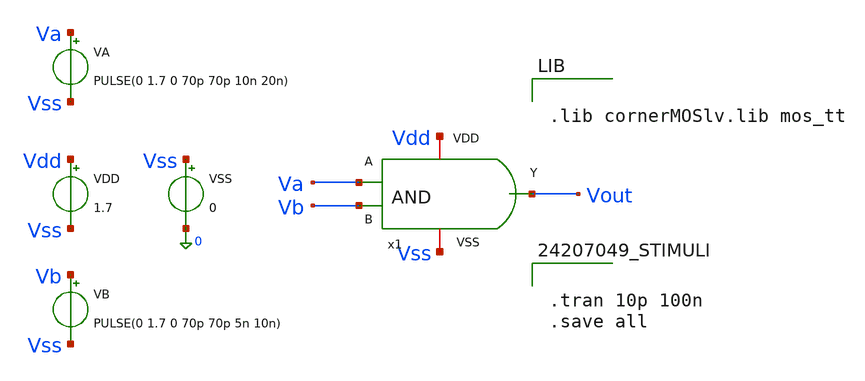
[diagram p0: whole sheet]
** sch_path: logic_gate/AND2/PRE-SIMULATION/AND_test.sch
**.subckt AND_test
VDD Vdd Vss 1.7
VSS Vss 0 0
VA Va Vss PULSE(0 1.7 0 70p 70p 10n 20n)
VB Vb Vss PULSE(0 1.7 0 70p 70p 5n 10n)
x1 Vdd Vout Va Vb Vss AND
**** begin user architecture code


.lib cornerMOSlv.lib mos_tt




.tran 10p 100n
.save all


**** end user architecture code
**.ends

* expanding   symbol:  AND.sym # of pins=5
** sym_path: logic_gate/AND2/PRE-SIMULATION/AND.sym
** sch_path: logic_gate/AND2/PRE-SIMULATION/AND.sch
.subckt AND VDD Y A B VSS
*.ipin A
*.ipin B
*.opin Y
*.iopin VDD
*.iopin VSS
XM1 net1 A net2 VSS sg13_lv_nmos w=0.15u l=0.13u ng=1 m=1 mm_ok=1
XM2 net1 A VDD VDD sg13_lv_pmos w=0.15u l=0.13u ng=1 m=1 mm_ok=1
XM3 net1 B VDD VDD sg13_lv_pmos w=0.15u l=0.13u ng=1 m=1 mm_ok=1
XM4 net2 B VSS VSS sg13_lv_nmos w=0.15u l=0.13u ng=1 m=1 mm_ok=1
XM5 Y net1 VDD VDD sg13_lv_pmos w=0.15u l=0.13u ng=1 m=1 mm_ok=1
XM6 Y net1 VSS VSS sg13_lv_nmos w=0.15u l=0.13u ng=1 m=1 mm_ok=1
.ends

.end
